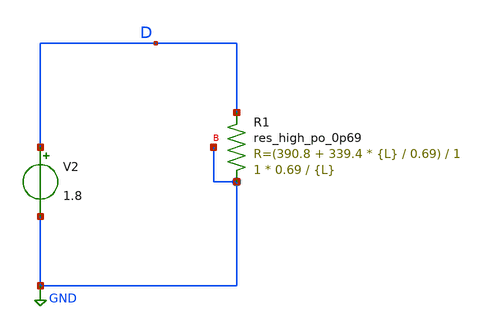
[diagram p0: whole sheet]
** sch_path: sky130A/xschem_libs/sky130_tests_ase/test_sweep_res_l/schematic/test_sweep_res_l.sch
* Copyright 2021 Stefan Frederik Schippers
* Licensed under the Apache License, Version 2.0 (the "License");
* you may not use this file except in compliance with the License.
* You may obtain a copy of the License at
* https://www.apache.org/licenses/LICENSE-2.0
* Unless required by applicable law or agreed to in writing, software
* distributed under the License is distributed on an "AS IS" BASIS,
* WITHOUT WARRANTIES OR CONDITIONS OF ANY KIND, either express or implied.
* See the License for the specific language governing permissions and
* limitations under the License.
**.subckt test_sweep_res_l
V2 D GND 1.8
XR1 GND D GND sky130_fd_pr__res_high_po_0p69 L={L} mult=1 m=1
**.ends
.GLOBAL GND
.end
